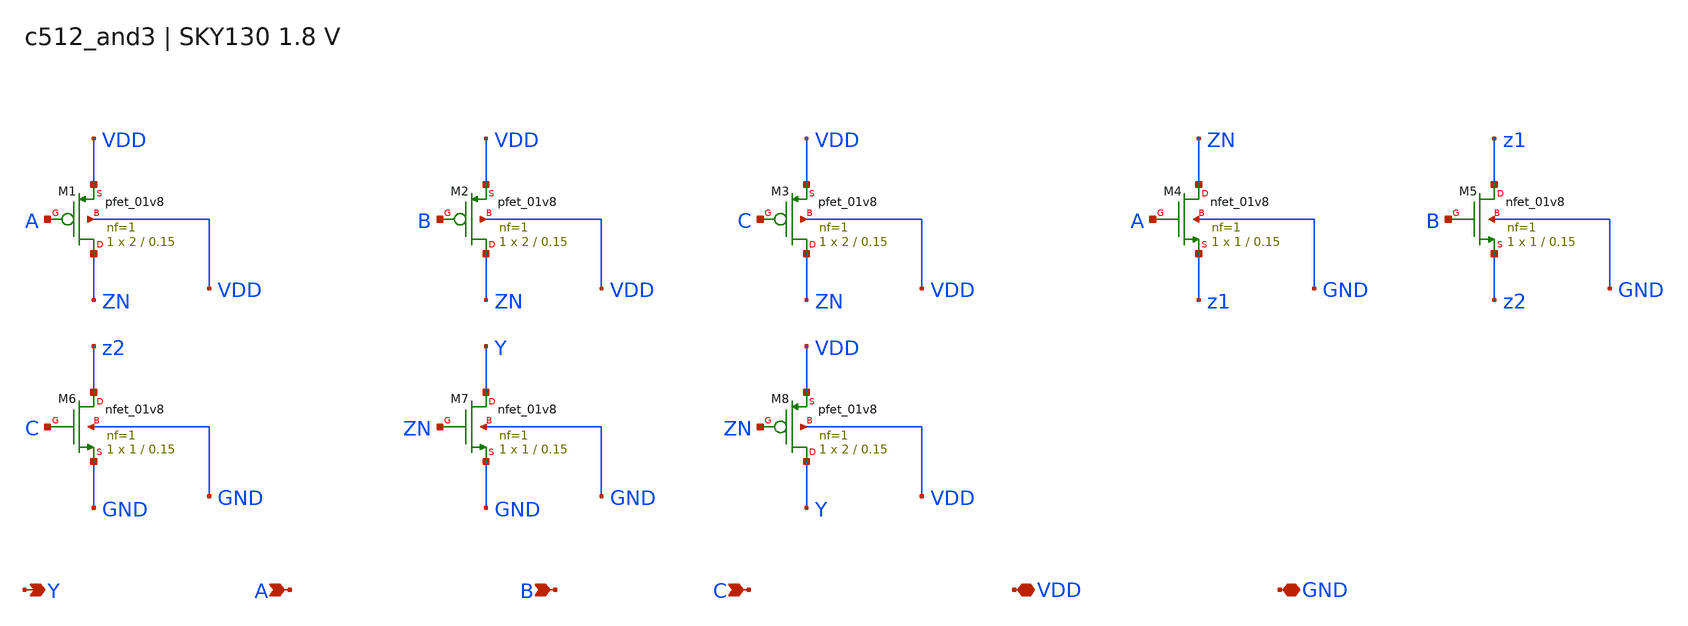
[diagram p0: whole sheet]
** sch_path: c512_and3.sch
**.subckt c512_and3 Y A B C VDD GND
*.opin Y
*.ipin A
*.ipin B
*.ipin C
*.iopin VDD
*.iopin GND
XM1 ZN A VDD VDD sky130_fd_pr__pfet_01v8 L=0.15 W=2 nf=1 ad=0.58 as=0.58 pd=4.58 ps=4.58 nrd=0.145
+ nrs=0.145 sa=0 sb=0 sd=0 mult=1 m=1
XM2 ZN B VDD VDD sky130_fd_pr__pfet_01v8 L=0.15 W=2 nf=1 ad=0.58 as=0.58 pd=4.58 ps=4.58 nrd=0.145
+ nrs=0.145 sa=0 sb=0 sd=0 mult=1 m=1
XM3 ZN C VDD VDD sky130_fd_pr__pfet_01v8 L=0.15 W=2 nf=1 ad=0.58 as=0.58 pd=4.58 ps=4.58 nrd=0.145
+ nrs=0.145 sa=0 sb=0 sd=0 mult=1 m=1
XM4 ZN A z1 GND sky130_fd_pr__nfet_01v8 L=0.15 W=1 nf=1 ad=0.29 as=0.29 pd=2.58 ps=2.58 nrd=0.29
+ nrs=0.29 sa=0 sb=0 sd=0 mult=1 m=1
XM5 z1 B z2 GND sky130_fd_pr__nfet_01v8 L=0.15 W=1 nf=1 ad=0.29 as=0.29 pd=2.58 ps=2.58 nrd=0.29
+ nrs=0.29 sa=0 sb=0 sd=0 mult=1 m=1
XM6 z2 C GND GND sky130_fd_pr__nfet_01v8 L=0.15 W=1 nf=1 ad=0.29 as=0.29 pd=2.58 ps=2.58 nrd=0.29
+ nrs=0.29 sa=0 sb=0 sd=0 mult=1 m=1
XM7 Y ZN GND GND sky130_fd_pr__nfet_01v8 L=0.15 W=1 nf=1 ad=0.29 as=0.29 pd=2.58 ps=2.58 nrd=0.29
+ nrs=0.29 sa=0 sb=0 sd=0 mult=1 m=1
XM8 Y ZN VDD VDD sky130_fd_pr__pfet_01v8 L=0.15 W=2 nf=1 ad=0.58 as=0.58 pd=4.58 ps=4.58 nrd=0.145
+ nrs=0.145 sa=0 sb=0 sd=0 mult=1 m=1
**.ends
.end
